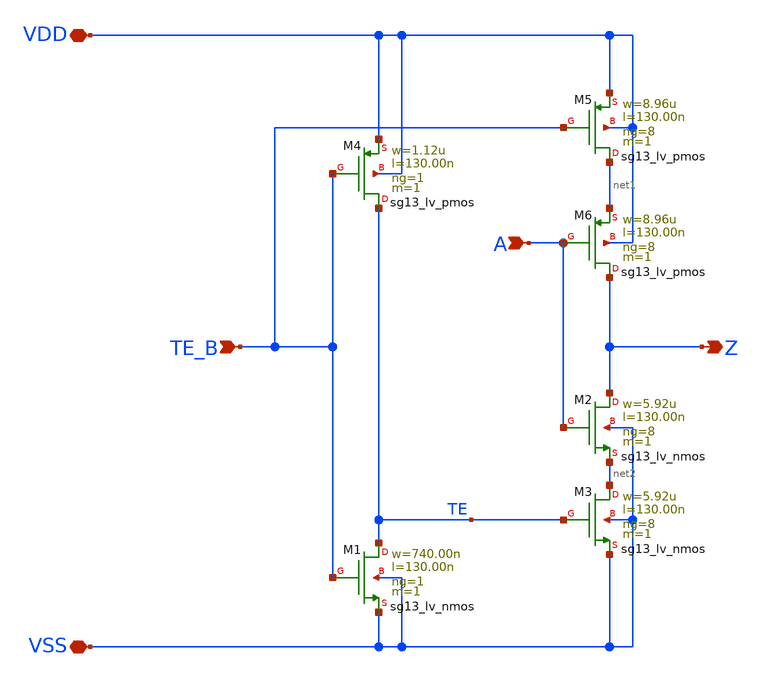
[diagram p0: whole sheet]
** sch_path: ihp-sg13g2/libs.tech/xschem/sg13g2_stdcells/sg13g2_einvn_8.sch
**.subckt sg13g2_einvn_8 TE_B A Z VDD VSS
*.ipin TE_B
*.ipin A
*.opin Z
*.iopin VDD
*.iopin VSS
XM1 TE TE_B VSS VSS sg13_lv_nmos w=740.00n l=130.00n ng=1 m=1 mm_ok=1
XM2 Z A net2 VSS sg13_lv_nmos w=5.92u l=130.00n ng=8 m=1 mm_ok=1
XM3 net2 TE VSS VSS sg13_lv_nmos w=5.92u l=130.00n ng=8 m=1 mm_ok=1
XM4 TE TE_B VDD VDD sg13_lv_pmos w=1.12u l=130.00n ng=1 m=1 mm_ok=1
XM5 net1 TE_B VDD VDD sg13_lv_pmos w=8.96u l=130.00n ng=8 m=1 mm_ok=1
XM6 Z A net1 VDD sg13_lv_pmos w=8.96u l=130.00n ng=8 m=1 mm_ok=1
**.ends
.end
